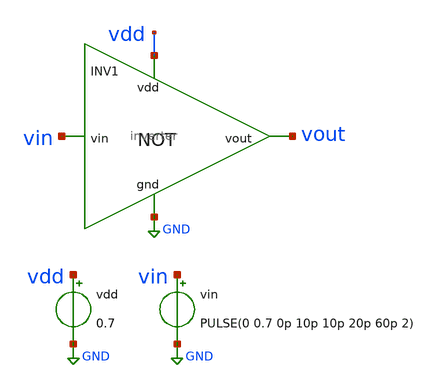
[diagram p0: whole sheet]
** sch_path: Xschem_ASAP7/inverter_test.sch
**.subckt inverter_test
x1 vdd vin vout GND inverter
vdd vdd GND 0.7
vin vin GND PULSE(0 0.7 0p 10p 10p 20p 60p 2)
**** begin user architecture code



.control
run
set filetype=ascii
set appendwrite

echo "WPfet,WNfet,Vm,Id,Gain,NMH,NML,Gm,tpd,tRise,tFall,Fsw,Power,Rout" > results.csv
let wpfet = 6
foreach wpfet 14 13 12 11 10 9 8 7 6 5 4 3 2
	foreach wnfet 14 13 12 11 10 9 8 7 6 5 4 3 2
		alter n.x1.xpfet1.npmos_finfet nfin = $wpfet
      		alter n.x1.xnfet1.nnmos_finfet nfin = $wnfet
		show n.x1.xpfet1.npmos_finfet : nfin
      		show n.x1.xnfet1.nnmos_finfet : nfin

		dc vin 0 0.7 1m

		set brushwidth 3

		setplot dc
		*plot vin vout
		meas dc vm when vin=vout

		if $&dc.vm > 0.34
			if $&dc.vm < 0.36

				let id = abs(vdd#branch)
				meas dc id_max MAX id
				print id_max

				let gm = real(deriv(id, vin))
				meas dc gm_max MAX gm
				print gm_max

				let rout = abs(real(deriv(vout, id)))
				meas dc rout_max MAX rout
				print rout_max

				let gain = abs(deriv(vout))
				meas dc gain_max MAX gain
				let gain_scaled = (gain >= 1)*0.7
				*plot gain_scaled vout
				meas dc vil find vin when gain_scaled=0.7 cross=1
				meas dc vih find vin when gain_scaled=0.7 cross=last
				let vol = 0
				let voh = 0.7
				let nmh = voh-vih
				let nml = vil-vol
				print nmh
				print nml

				tran 0.02p 125p
				setplot tran

				*plot vin vout
				meas tran tin_rise50 when vin=0.35 RISE=2
				meas tran tout_fall50 when vout=0.35 FALL=2
				meas tran tin_fall50 when vin=0.35 FALL=2
				meas tran tout_rise50 when vout=0.35 RISE=2
				meas tran tout_rise10 when vout=0.07 RISE=2
				meas tran tout_rise90 when vout=0.63 RISE=2
				meas tran tout_fall10 when vout=0.07 FALL=2
				meas tran tout_fall90 when vout=0.63 FALL=2

				let tpHL = tout_fall50-tin_rise50
				let tpLH = tout_rise50-tin_fall50
				let tpd = (tpHL+tpLH)/2
				let tr = tout_rise90 - tout_rise10
				let tf = tout_fall10 - tout_fall90
				let fsw = 1/(tr+tf)
				let id_tran = vdd#branch
				*plot id*1000 vout
				meas tran id_integ integ id_tran from=60e-12 to=120e-12
				let power_int = id_integ*0.7
				let power = abs(power_int/60)

				print tpHL
				print tpLH
				print tpd
				print tr
				print tf
				print fsw
				print power


				echo
+ "$wpfet,$wnfet,$&dc.vm,$&dc.id_max,$&dc.gain_max,$&dc.nmh,$&dc.nml,$&dc.gm_max,$&tran.tpd,$&tran.tr,$&tran.tf,$&tran.fsw,$&tran.power,$&dc.rout_max" >> results.csv
			end
		end
   	end
	*$&wpfet = $&wpfet-1
end


.endc
.save all
.end


**** end user architecture code
**.ends

* expanding   symbol:  inverter.sym # of pins=4
** sym_path: Xschem_ASAP7/inverter.sym
** sch_path: Xschem_ASAP7/inverter.sch
.subckt inverter vdd vin vout gnd
*.ipin vin
*.ipin vdd
*.ipin gnd
*.opin vout
Xnfet1 vout vin gnd gnd asap_7nm_nfet l=7e-009 nfin=13
Xpfet1 vout vin vdd vout asap_7nm_pfet l=7e-009 nfin=14
.ends

.GLOBAL GND
.end
